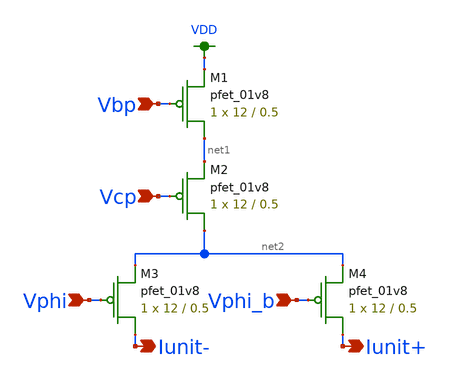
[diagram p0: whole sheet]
** sch_path: simulation/dac/dac_unit.sch
**.subckt dac_unit Vphi Vbp Vcp Iunit- Iunit+ Vphi_b
*.ipin Vphi
*.ipin Vbp
*.ipin Vcp
*.opin Iunit-
*.opin Iunit+
*.ipin Vphi_b
XM1 net1 Vbp VDD VDD sky130_fd_pr__pfet_01v8 L=0.5 W=12 nf=1 ad='int((nf+1)/2) * W/nf * 0.29' as='int((nf+2)/2) * W/nf * 0.29'
+ pd='2*int((nf+1)/2) * (W/nf + 0.29)' ps='2*int((nf+2)/2) * (W/nf + 0.29)' nrd='0.29 / W' nrs='0.29 / W'
+ sa=0 sb=0 sd=0 mult=1 m=1
XM2 net2 Vcp net1 VDD sky130_fd_pr__pfet_01v8 L=0.5 W=12 nf=1 ad='int((nf+1)/2) * W/nf * 0.29' as='int((nf+2)/2) * W/nf * 0.29'
+ pd='2*int((nf+1)/2) * (W/nf + 0.29)' ps='2*int((nf+2)/2) * (W/nf + 0.29)' nrd='0.29 / W' nrs='0.29 / W'
+ sa=0 sb=0 sd=0 mult=1 m=1
XM3 Iunit- Vphi net2 VDD sky130_fd_pr__pfet_01v8 L=0.5 W=12 nf=1 ad='int((nf+1)/2) * W/nf * 0.29' as='int((nf+2)/2) * W/nf * 0.29'
+ pd='2*int((nf+1)/2) * (W/nf + 0.29)' ps='2*int((nf+2)/2) * (W/nf + 0.29)' nrd='0.29 / W' nrs='0.29 / W'
+ sa=0 sb=0 sd=0 mult=1 m=1
XM4 Iunit+ Vphi_b net2 VDD sky130_fd_pr__pfet_01v8 L=0.5 W=12 nf=1 ad='int((nf+1)/2) * W/nf * 0.29' as='int((nf+2)/2) * W/nf * 0.29'
+ pd='2*int((nf+1)/2) * (W/nf + 0.29)' ps='2*int((nf+2)/2) * (W/nf + 0.29)' nrd='0.29 / W' nrs='0.29 / W'
+ sa=0 sb=0 sd=0 mult=1 m=1
**.ends
.GLOBAL VDD
.end
